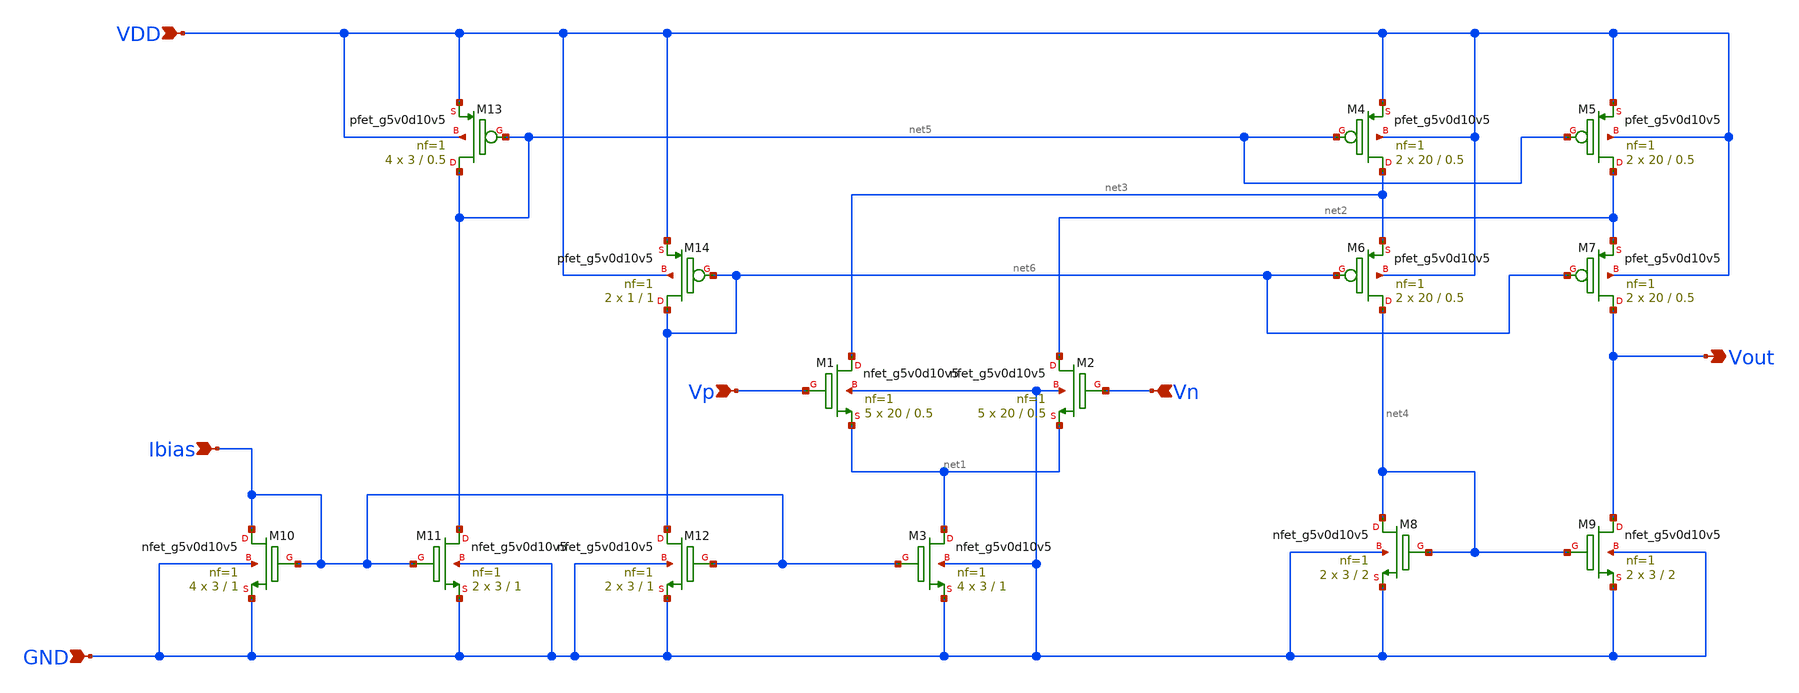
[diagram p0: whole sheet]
** sch_path: Analog_blocks/Analog_Blocks/OTA/Schematic/Folded_Cascode_OTA/Transitor5v/Folded_Cascode_OTA_5v.sch
**.subckt Folded_Cascode_OTA_5v VDD GND Vp Vn Vout Ibias
*.ipin VDD
*.ipin GND
*.ipin Vp
*.ipin Vn
*.opin Vout
*.ipin Ibias
XM1 net3 Vp net1 GND sky130_fd_pr__nfet_g5v0d10v5 L=0.5 W=20 nf=1 ad='int((nf+1)/2) * W/nf * 0.29' as='int((nf+2)/2) * W/nf * 0.29'
+ pd='2*int((nf+1)/2) * (W/nf + 0.29)' ps='2*int((nf+2)/2) * (W/nf + 0.29)' nrd='0.29 / W' nrs='0.29 / W'
+ sa=0 sb=0 sd=0 mult=5 m=5
XM2 net2 Vn net1 GND sky130_fd_pr__nfet_g5v0d10v5 L=0.5 W=20 nf=1 ad='int((nf+1)/2) * W/nf * 0.29' as='int((nf+2)/2) * W/nf * 0.29'
+ pd='2*int((nf+1)/2) * (W/nf + 0.29)' ps='2*int((nf+2)/2) * (W/nf + 0.29)' nrd='0.29 / W' nrs='0.29 / W'
+ sa=0 sb=0 sd=0 mult=5 m=5
XM9 Vout net4 GND GND sky130_fd_pr__nfet_g5v0d10v5 L=2 W=3 nf=1 ad='int((nf+1)/2) * W/nf * 0.29' as='int((nf+2)/2) * W/nf * 0.29'
+ pd='2*int((nf+1)/2) * (W/nf + 0.29)' ps='2*int((nf+2)/2) * (W/nf + 0.29)' nrd='0.29 / W' nrs='0.29 / W'
+ sa=0 sb=0 sd=0 mult=2 m=2
XM6 net4 net6 net3 VDD sky130_fd_pr__pfet_g5v0d10v5 L=0.5 W=20 nf=1 ad='int((nf+1)/2) * W/nf * 0.29'
+ as='int((nf+2)/2) * W/nf * 0.29' pd='2*int((nf+1)/2) * (W/nf + 0.29)' ps='2*int((nf+2)/2) * (W/nf + 0.29)'
+ nrd='0.29 / W' nrs='0.29 / W' sa=0 sb=0 sd=0 mult=2 m=2
XM5 net2 net5 VDD VDD sky130_fd_pr__pfet_g5v0d10v5 L=0.5 W=20 nf=1 ad='int((nf+1)/2) * W/nf * 0.29' as='int((nf+2)/2) * W/nf * 0.29'
+ pd='2*int((nf+1)/2) * (W/nf + 0.29)' ps='2*int((nf+2)/2) * (W/nf + 0.29)' nrd='0.29 / W' nrs='0.29 / W'
+ sa=0 sb=0 sd=0 mult=2 m=2
XM4 net3 net5 VDD VDD sky130_fd_pr__pfet_g5v0d10v5 L=0.5 W=20 nf=1 ad='int((nf+1)/2) * W/nf * 0.29' as='int((nf+2)/2) * W/nf * 0.29'
+ pd='2*int((nf+1)/2) * (W/nf + 0.29)' ps='2*int((nf+2)/2) * (W/nf + 0.29)' nrd='0.29 / W' nrs='0.29 / W'
+ sa=0 sb=0 sd=0 mult=2 m=2
XM3 net1 Ibias GND GND sky130_fd_pr__nfet_g5v0d10v5 L=1 W=3 nf=1 ad='int((nf+1)/2) * W/nf * 0.29' as='int((nf+2)/2) * W/nf * 0.29'
+ pd='2*int((nf+1)/2) * (W/nf + 0.29)' ps='2*int((nf+2)/2) * (W/nf + 0.29)' nrd='0.29 / W' nrs='0.29 / W'
+ sa=0 sb=0 sd=0 mult=4 m=4
XM7 Vout net6 net2 VDD sky130_fd_pr__pfet_g5v0d10v5 L=0.5 W=20 nf=1 ad='int((nf+1)/2) * W/nf * 0.29'
+ as='int((nf+2)/2) * W/nf * 0.29' pd='2*int((nf+1)/2) * (W/nf + 0.29)' ps='2*int((nf+2)/2) * (W/nf + 0.29)'
+ nrd='0.29 / W' nrs='0.29 / W' sa=0 sb=0 sd=0 mult=2 m=2
XM8 net4 net4 GND GND sky130_fd_pr__nfet_g5v0d10v5 L=2 W=3 nf=1 ad='int((nf+1)/2) * W/nf * 0.29' as='int((nf+2)/2) * W/nf * 0.29'
+ pd='2*int((nf+1)/2) * (W/nf + 0.29)' ps='2*int((nf+2)/2) * (W/nf + 0.29)' nrd='0.29 / W' nrs='0.29 / W'
+ sa=0 sb=0 sd=0 mult=2 m=2
XM10 Ibias Ibias GND GND sky130_fd_pr__nfet_g5v0d10v5 L=1 W=3 nf=1 ad='int((nf+1)/2) * W/nf * 0.29' as='int((nf+2)/2) * W/nf * 0.29'
+ pd='2*int((nf+1)/2) * (W/nf + 0.29)' ps='2*int((nf+2)/2) * (W/nf + 0.29)' nrd='0.29 / W' nrs='0.29 / W'
+ sa=0 sb=0 sd=0 mult=4 m=4
XM11 net5 Ibias GND GND sky130_fd_pr__nfet_g5v0d10v5 L=1 W=3 nf=1 ad='int((nf+1)/2) * W/nf * 0.29' as='int((nf+2)/2) * W/nf * 0.29'
+ pd='2*int((nf+1)/2) * (W/nf + 0.29)' ps='2*int((nf+2)/2) * (W/nf + 0.29)' nrd='0.29 / W' nrs='0.29 / W'
+ sa=0 sb=0 sd=0 mult=2 m=2
XM12 net6 Ibias GND GND sky130_fd_pr__nfet_g5v0d10v5 L=1 W=3 nf=1 ad='int((nf+1)/2) * W/nf * 0.29' as='int((nf+2)/2) * W/nf * 0.29'
+ pd='2*int((nf+1)/2) * (W/nf + 0.29)' ps='2*int((nf+2)/2) * (W/nf + 0.29)' nrd='0.29 / W' nrs='0.29 / W'
+ sa=0 sb=0 sd=0 mult=2 m=2
XM13 net5 net5 VDD VDD sky130_fd_pr__pfet_g5v0d10v5 L=0.5 W=3 nf=1 ad='int((nf+1)/2) * W/nf * 0.29' as='int((nf+2)/2) * W/nf * 0.29'
+ pd='2*int((nf+1)/2) * (W/nf + 0.29)' ps='2*int((nf+2)/2) * (W/nf + 0.29)' nrd='0.29 / W' nrs='0.29 / W'
+ sa=0 sb=0 sd=0 mult=4 m=4
XM14 net6 net6 VDD VDD sky130_fd_pr__pfet_g5v0d10v5 L=1 W=1 nf=1 ad='int((nf+1)/2) * W/nf * 0.29' as='int((nf+2)/2) * W/nf * 0.29'
+ pd='2*int((nf+1)/2) * (W/nf + 0.29)' ps='2*int((nf+2)/2) * (W/nf + 0.29)' nrd='0.29 / W' nrs='0.29 / W'
+ sa=0 sb=0 sd=0 mult=2 m=2
**.ends
.end
